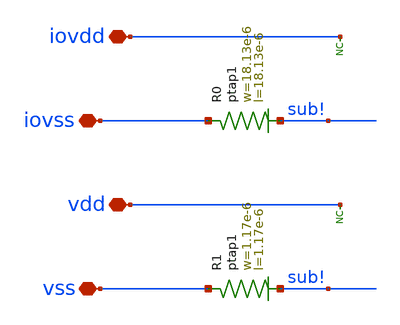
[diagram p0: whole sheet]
** sch_path: ihp-sg13g2/libs.ref/sg13g2_io/sch/xschem/sg13g2_Filler1000.sch
**.subckt sg13g2_Filler1000 iovdd iovss vdd vss
*.iopin iovdd
*.iopin iovss
*.iopin vdd
*.iopin vss
* noconn iovdd
* noconn vdd
XR0 iovss sub! ptap1 R=2.443 w=18.13e-6 l=18.13e-6
XR1 vss sub! ptap1 R=162 w=1.17e-6 l=1.17e-6
**.ends
.end
